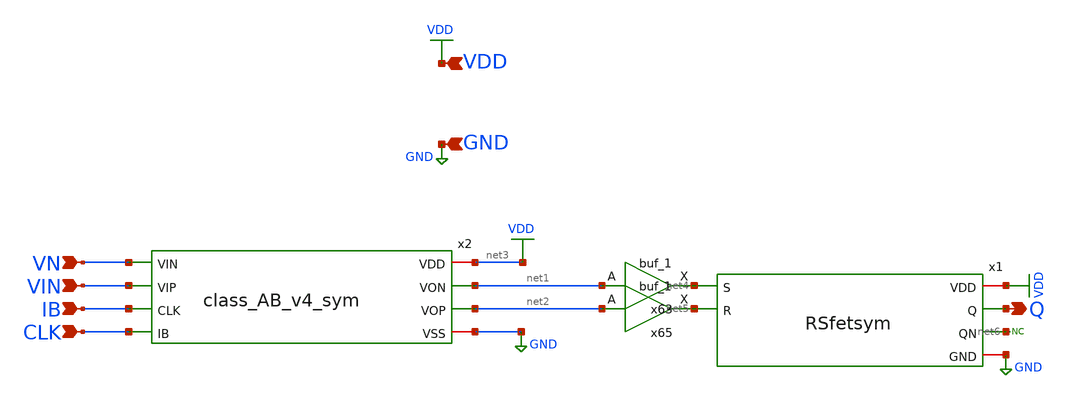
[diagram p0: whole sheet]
** sch_path: flashADC/xschem/frontAnalog_v0p0p1.sch
.lib $::SKYWATER_MODELS/sky130.lib.spice tt
.include $::SKYWATER_STDCELLS/sky130_fd_sc_hd.spice

**.subckt frontAnalog_v0p0p1 VDD GND VN VIN IB CLK Q
*.ipin VDD
*.ipin GND
*.ipin VN
*.ipin VIN
*.ipin IB
*.ipin CLK
*.opin Q
x63 net1 GND GND VDD VDD net4 sky130_fd_sc_hd__buf_1
x65 net2 GND GND VDD VDD net5 sky130_fd_sc_hd__buf_1
* noconn #net6
x1 VDD net4 net5 Q net6 GND RSfetsym
x2 net3 net1 net2 VN VIN IB CLK GND class_AB_v4_sym
**.ends

* expanding   symbol:  /foss/designs/Analog_FA23_SP24/RSlatch/xschem/RSfetsym.sym # of pins=6
** sym_path: RSlatch/xschem/RSfetsym.sym
** sch_path: RSlatch/xschem/RSfetsym.sch
.subckt RSfetsym VDD S R Q QN GND
*.opin Q
*.opin QN
*.ipin S
*.ipin R
*.iopin VDD
*.iopin GND
XM1 Q S net1 GND sky130_fd_pr__nfet_01v8 L=0.15 W=1 nf=1 ad='int((nf+1)/2) * W/nf * 0.29' as='int((nf+2)/2) * W/nf * 0.29'
+ pd='2*int((nf+1)/2) * (W/nf + 0.29)' ps='2*int((nf+2)/2) * (W/nf + 0.29)' nrd='0.29 / W' nrs='0.29 / W'
+ sa=0 sb=0 sd=0 mult=1 m=1
XM2 net1 QN GND GND sky130_fd_pr__nfet_01v8 L=0.15 W=1 nf=1 ad='int((nf+1)/2) * W/nf * 0.29' as='int((nf+2)/2) * W/nf * 0.29'
+ pd='2*int((nf+1)/2) * (W/nf + 0.29)' ps='2*int((nf+2)/2) * (W/nf + 0.29)' nrd='0.29 / W' nrs='0.29 / W'
+ sa=0 sb=0 sd=0 mult=1 m=1
XM3 QN R net2 GND sky130_fd_pr__nfet_01v8 L=0.15 W=1 nf=1 ad='int((nf+1)/2) * W/nf * 0.29' as='int((nf+2)/2) * W/nf * 0.29'
+ pd='2*int((nf+1)/2) * (W/nf + 0.29)' ps='2*int((nf+2)/2) * (W/nf + 0.29)' nrd='0.29 / W' nrs='0.29 / W'
+ sa=0 sb=0 sd=0 mult=1 m=1
XM4 net2 Q GND GND sky130_fd_pr__nfet_01v8 L=0.15 W=1 nf=1 ad='int((nf+1)/2) * W/nf * 0.29' as='int((nf+2)/2) * W/nf * 0.29'
+ pd='2*int((nf+1)/2) * (W/nf + 0.29)' ps='2*int((nf+2)/2) * (W/nf + 0.29)' nrd='0.29 / W' nrs='0.29 / W'
+ sa=0 sb=0 sd=0 mult=1 m=1
XM5 Q QN VDD VDD sky130_fd_pr__pfet_01v8 L=0.30 W=2 nf=1 ad='int((nf+1)/2) * W/nf * 0.29' as='int((nf+2)/2) * W/nf * 0.29'
+ pd='2*int((nf+1)/2) * (W/nf + 0.29)' ps='2*int((nf+2)/2) * (W/nf + 0.29)' nrd='0.29 / W' nrs='0.29 / W'
+ sa=0 sb=0 sd=0 mult=1 m=1
XM6 QN Q VDD VDD sky130_fd_pr__pfet_01v8 L=0.30 W=2 nf=1 ad='int((nf+1)/2) * W/nf * 0.29' as='int((nf+2)/2) * W/nf * 0.29'
+ pd='2*int((nf+1)/2) * (W/nf + 0.29)' ps='2*int((nf+2)/2) * (W/nf + 0.29)' nrd='0.29 / W' nrs='0.29 / W'
+ sa=0 sb=0 sd=0 mult=1 m=1
XM7 Q S VDD VDD sky130_fd_pr__pfet_01v8 L=0.25 W=4 nf=2 ad='int((nf+1)/2) * W/nf * 0.29' as='int((nf+2)/2) * W/nf * 0.29'
+ pd='2*int((nf+1)/2) * (W/nf + 0.29)' ps='2*int((nf+2)/2) * (W/nf + 0.29)' nrd='0.29 / W' nrs='0.29 / W'
+ sa=0 sb=0 sd=0 mult=1 m=1
XM8 QN R VDD VDD sky130_fd_pr__pfet_01v8 L=0.25 W=4 nf=2 ad='int((nf+1)/2) * W/nf * 0.29' as='int((nf+2)/2) * W/nf * 0.29'
+ pd='2*int((nf+1)/2) * (W/nf + 0.29)' ps='2*int((nf+2)/2) * (W/nf + 0.29)' nrd='0.29 / W' nrs='0.29 / W'
+ sa=0 sb=0 sd=0 mult=1 m=1
XM9 Q net3 GND GND sky130_fd_pr__nfet_01v8 L=0.25 W=2 nf=1 ad='int((nf+1)/2) * W/nf * 0.29' as='int((nf+2)/2) * W/nf * 0.29'
+ pd='2*int((nf+1)/2) * (W/nf + 0.29)' ps='2*int((nf+2)/2) * (W/nf + 0.29)' nrd='0.29 / W' nrs='0.29 / W'
+ sa=0 sb=0 sd=0 mult=1 m=1
XM10 QN net4 GND GND sky130_fd_pr__nfet_01v8 L=0.25 W=2 nf=1 ad='int((nf+1)/2) * W/nf * 0.29' as='int((nf+2)/2) * W/nf * 0.29'
+ pd='2*int((nf+1)/2) * (W/nf + 0.29)' ps='2*int((nf+2)/2) * (W/nf + 0.29)' nrd='0.29 / W' nrs='0.29 / W'
+ sa=0 sb=0 sd=0 mult=1 m=1
x2 R GND GND VDD VDD net3 sky130_fd_sc_hd__inv_4
x1 S GND GND VDD VDD net4 sky130_fd_sc_hd__inv_4
.ends


* expanding   symbol:  /foss/designs/Analog_FA23_SP24/strongARM/class_AB_v4_sym.sym # of pins=8
** sym_path: ComparatorLayout/xschem/class_AB_v4_sym.sym
** sch_path: ComparatorLayout/xschem/class_AB_v4_sym.sch
.subckt class_AB_v4_sym VDD VON VOP VIN VIP CLK IB VSS
*.iopin VDD
*.ipin IB
*.iopin VSS
*.ipin VIP
*.ipin VIN
*.opin VON
*.opin VOP
*.ipin CLK
XM17 net3 VIP VIR VSS sky130_fd_pr__nfet_01v8_lvt L=0.6 W=4 nf=1 ad='int((nf+1)/2) * W/nf * 0.29' as='int((nf+2)/2) * W/nf * 0.29'
+ pd='2*int((nf+1)/2) * (W/nf + 0.29)' ps='2*int((nf+2)/2) * (W/nf + 0.29)' nrd='0.29 / W' nrs='0.29 / W'
+ sa=0 sb=0 sd=0 mult=1 m=1
XM15 net2 VIN VIR VSS sky130_fd_pr__nfet_01v8_lvt L=0.6 W=4 nf=1 ad='int((nf+1)/2) * W/nf * 0.29' as='int((nf+2)/2) * W/nf * 0.29'
+ pd='2*int((nf+1)/2) * (W/nf + 0.29)' ps='2*int((nf+2)/2) * (W/nf + 0.29)' nrd='0.29 / W' nrs='0.29 / W'
+ sa=0 sb=0 sd=0 mult=1 m=1
XM13 VIR IB VSS VSS sky130_fd_pr__nfet_01v8_lvt L=0.6 W=4 nf=1 ad='int((nf+1)/2) * W/nf * 0.29' as='int((nf+2)/2) * W/nf * 0.29'
+ pd='2*int((nf+1)/2) * (W/nf + 0.29)' ps='2*int((nf+2)/2) * (W/nf + 0.29)' nrd='0.29 / W' nrs='0.29 / W'
+ sa=0 sb=0 sd=0 mult=2 m=2
XM6 VON VOP VDD VDD sky130_fd_pr__pfet_01v8_lvt L=0.35 W=4 nf=1 ad='int((nf+1)/2) * W/nf * 0.29' as='int((nf+2)/2) * W/nf * 0.29'
+ pd='2*int((nf+1)/2) * (W/nf + 0.29)' ps='2*int((nf+2)/2) * (W/nf + 0.29)' nrd='0.29 / W' nrs='0.29 / W'
+ sa=0 sb=0 sd=0 mult=1 m=1
XM7 VOP VON VDD VDD sky130_fd_pr__pfet_01v8_lvt L=0.35 W=4 nf=1 ad='int((nf+1)/2) * W/nf * 0.29' as='int((nf+2)/2) * W/nf * 0.29'
+ pd='2*int((nf+1)/2) * (W/nf + 0.29)' ps='2*int((nf+2)/2) * (W/nf + 0.29)' nrd='0.29 / W' nrs='0.29 / W'
+ sa=0 sb=0 sd=0 mult=1 m=1
XM10 VOP VON net1 VSS sky130_fd_pr__nfet_01v8_lvt L=0.15 W=1 nf=1 ad='int((nf+1)/2) * W/nf * 0.29' as='int((nf+2)/2) * W/nf * 0.29'
+ pd='2*int((nf+1)/2) * (W/nf + 0.29)' ps='2*int((nf+2)/2) * (W/nf + 0.29)' nrd='0.29 / W' nrs='0.29 / W'
+ sa=0 sb=0 sd=0 mult=1 m=1
XM11 VON VOP net1 VSS sky130_fd_pr__nfet_01v8_lvt L=0.15 W=1 nf=1 ad='int((nf+1)/2) * W/nf * 0.29' as='int((nf+2)/2) * W/nf * 0.29'
+ pd='2*int((nf+1)/2) * (W/nf + 0.29)' ps='2*int((nf+2)/2) * (W/nf + 0.29)' nrd='0.29 / W' nrs='0.29 / W'
+ sa=0 sb=0 sd=0 mult=1 m=1
XM1 net1 CLK VSS VSS sky130_fd_pr__nfet_01v8_lvt L=0.15 W=1 nf=1 ad='int((nf+1)/2) * W/nf * 0.29' as='int((nf+2)/2) * W/nf * 0.29'
+ pd='2*int((nf+1)/2) * (W/nf + 0.29)' ps='2*int((nf+2)/2) * (W/nf + 0.29)' nrd='0.29 / W' nrs='0.29 / W'
+ sa=0 sb=0 sd=0 mult=1 m=1
XM2 VOP CLK VON VDD sky130_fd_pr__pfet_01v8_lvt L=0.35 W=4 nf=1 ad='int((nf+1)/2) * W/nf * 0.29' as='int((nf+2)/2) * W/nf * 0.29'
+ pd='2*int((nf+1)/2) * (W/nf + 0.29)' ps='2*int((nf+2)/2) * (W/nf + 0.29)' nrd='0.29 / W' nrs='0.29 / W'
+ sa=0 sb=0 sd=0 mult=1 m=1
XM9 net2 CLK VOP VDD sky130_fd_pr__pfet_01v8_lvt L=0.35 W=4 nf=1 ad='int((nf+1)/2) * W/nf * 0.29' as='int((nf+2)/2) * W/nf * 0.29'
+ pd='2*int((nf+1)/2) * (W/nf + 0.29)' ps='2*int((nf+2)/2) * (W/nf + 0.29)' nrd='0.29 / W' nrs='0.29 / W'
+ sa=0 sb=0 sd=0 mult=1 m=1
XM14 net3 CLK VON VDD sky130_fd_pr__pfet_01v8_lvt L=0.35 W=4 nf=1 ad='int((nf+1)/2) * W/nf * 0.29' as='int((nf+2)/2) * W/nf * 0.29'
+ pd='2*int((nf+1)/2) * (W/nf + 0.29)' ps='2*int((nf+2)/2) * (W/nf + 0.29)' nrd='0.29 / W' nrs='0.29 / W'
+ sa=0 sb=0 sd=0 mult=1 m=1
XM3 VDD CLK net3 VSS sky130_fd_pr__nfet_01v8_lvt L=0.6 W=4 nf=1 ad='int((nf+1)/2) * W/nf * 0.29' as='int((nf+2)/2) * W/nf * 0.29'
+ pd='2*int((nf+1)/2) * (W/nf + 0.29)' ps='2*int((nf+2)/2) * (W/nf + 0.29)' nrd='0.29 / W' nrs='0.29 / W'
+ sa=0 sb=0 sd=0 mult=1 m=1
XM4 VDD CLK net2 VSS sky130_fd_pr__nfet_01v8_lvt L=0.6 W=4 nf=1 ad='int((nf+1)/2) * W/nf * 0.29' as='int((nf+2)/2) * W/nf * 0.29'
+ pd='2*int((nf+1)/2) * (W/nf + 0.29)' ps='2*int((nf+2)/2) * (W/nf + 0.29)' nrd='0.29 / W' nrs='0.29 / W'
+ sa=0 sb=0 sd=0 mult=1 m=1
XC1 VIP net2 VSS sky130_fd_pr__cap_var_lvt W=2 L=0.18 VM=1 m=1
XC2 VIN net3 VSS sky130_fd_pr__cap_var_lvt W=2 L=0.18 VM=1 m=1
.ends

.GLOBAL GND
.GLOBAL VDD
.end
